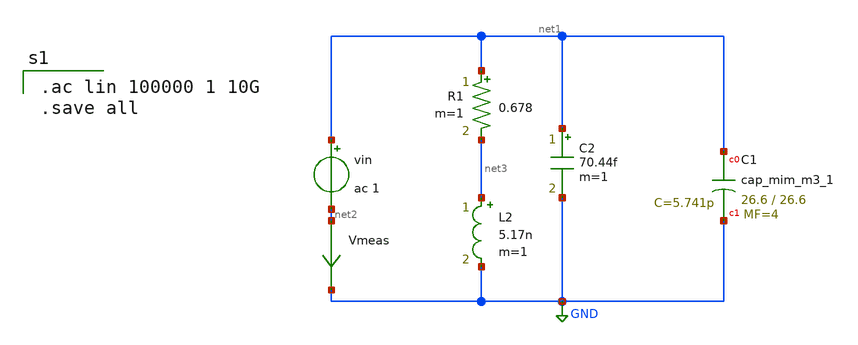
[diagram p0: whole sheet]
** sch_path: XSCHEM/ANTENNA/RLC_CSTXschem500.sch
**.subckt RLC_CSTXschem500
vin net1 net2 ac 1
XC1 net1 GND sky130_fd_pr__cap_mim_m3_1 W=26.6 L=26.6 MF=4 m=4
Vmeas net2 GND 0
.save i(vmeas)
R1 net1 net3 0.678 m=1
L2 net3 GND 5.17n m=1
C2 net1 GND 70.44f m=1
**** begin user architecture code

.ac lin 100000 1 10G
.save all


** opencircuitdesign pdks install
.lib $::SKYWATER_MODELS/sky130.lib.spice ff
.include /usr/local/share/pdk/sky130A/libs.ref/sky130_fd_sc_hd/spice/sky130_fd_sc_hd.spice

**** end user architecture code
**.ends
.GLOBAL GND
.end
